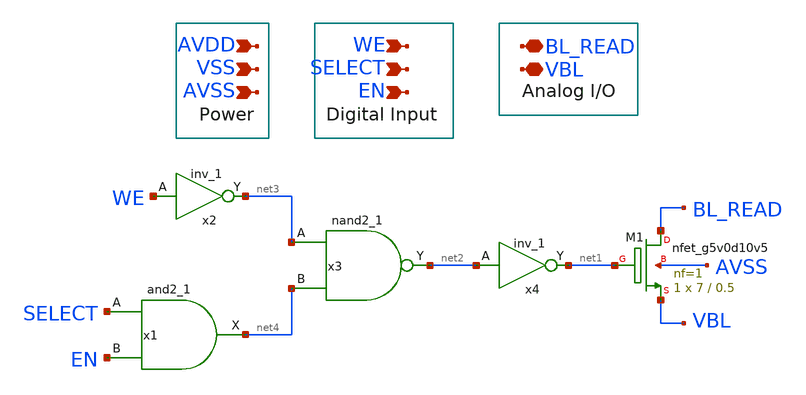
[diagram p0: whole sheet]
** sch_path: BL_Read_Interface/BL_read_mux.sch
**.subckt BL_read_mux AVSS BL_READ VBL AVDD VSS EN SELECT WE
*.ipin AVSS
*.iopin BL_READ
*.iopin VBL
*.ipin AVDD
*.ipin VSS
*.ipin EN
*.ipin SELECT
*.ipin WE
XM1 BL_READ net1 VBL AVSS sky130_fd_pr__nfet_g5v0d10v5 L=0.5 W=7 nf=1 ad='int((nf+1)/2) * W/nf * 0.29'
+ as='int((nf+2)/2) * W/nf * 0.29' pd='2*int((nf+1)/2) * (W/nf + 0.29)' ps='2*int((nf+2)/2) * (W/nf + 0.29)'
+ nrd='0.29 / W' nrs='0.29 / W' sa=0 sb=0 sd=0 mult=1 m=1
x1 SELECT EN VSS VSS AVDD AVDD net4 sky130_fd_sc_hd__and2_1
x2 WE VSS VSS AVDD AVDD net3 sky130_fd_sc_hd__inv_1
x3 net3 net4 VSS VSS AVDD AVDD net2 sky130_fd_sc_hd__nand2_1
x4 net2 VSS VSS AVDD AVDD net1 sky130_fd_sc_hd__inv_1
**.ends
.end
